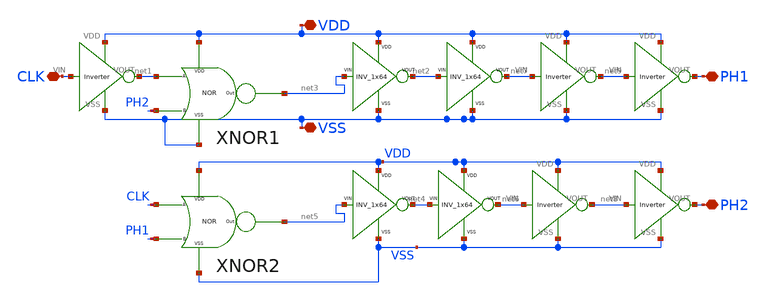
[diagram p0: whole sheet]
** sch_path: xschem/xschem_BGR_Top/Sigma_Delta/Non_over_clk/Non_over_clk.sch
**.subckt Non_over_clk VDD VSS CLK PH1 PH2
*.iopin VDD
*.iopin VSS
*.iopin CLK
*.iopin PH1
*.iopin PH2
X1 VSS VDD CLK net1 Inverter
X2 VSS VDD net9 PH1 Inverter
X3 VSS VDD net8 PH2 Inverter
X4 VSS VDD net3 net2 INV_1x64
X5 VSS VDD net5 net4 INV_1x64
XNOR1 VDD VSS net1 PH2 net3 NOR
XNOR2 VDD VSS CLK PH1 net5 NOR
X8 VSS VDD net6 net8 Inverter
X9 VSS VDD net7 net9 Inverter
X6 VSS VDD net2 net7 INV_1x64
X7 VSS VDD net4 net6 INV_1x64
**.ends

* expanding   symbol:  Sigma_Delta/Inverter/Inverter.sym # of pins=4
** sym_path: xschem/xschem_BGR_Top/Sigma_Delta/Inverter/Inverter.sym
** sch_path: xschem/xschem_BGR_Top/Sigma_Delta/Inverter/Inverter.sch
.subckt Inverter VSS VDD VIN VOUT
*.ipin VIN
*.iopin VDD
*.iopin VSS
*.opin VOUT
XM1 VOUT VIN VSS VSS sky130_fd_pr__nfet_01v8 L=0.15 W=0.9 nf=1 ad='int((nf+1)/2) * W/nf * 0.29' as='int((nf+2)/2) * W/nf * 0.29'
+ pd='2*int((nf+1)/2) * (W/nf + 0.29)' ps='2*int((nf+2)/2) * (W/nf + 0.29)' nrd='0.29 / W' nrs='0.29 / W'
+ sa=0 sb=0 sd=0 mult=1 m=1
XM2 VOUT VIN VDD VDD sky130_fd_pr__pfet_01v8 L=0.15 W=0.9 nf=2 ad='int((nf+1)/2) * W/nf * 0.29' as='int((nf+2)/2) * W/nf * 0.29'
+ pd='2*int((nf+1)/2) * (W/nf + 0.29)' ps='2*int((nf+2)/2) * (W/nf + 0.29)' nrd='0.29 / W' nrs='0.29 / W'
+ sa=0 sb=0 sd=0 mult=1 m=1
.ends


* expanding   symbol:  Sigma_Delta/INV_1x64/INV_1x64.sym # of pins=4
** sym_path: xschem/xschem_BGR_Top/Sigma_Delta/INV_1x64/INV_1x64.sym
** sch_path: xschem/xschem_BGR_Top/Sigma_Delta/INV_1x64/INV_1x64.sch
.subckt INV_1x64 VSS VDD VIN VOUT
*.ipin VIN
*.iopin VDD
*.iopin VSS
*.opin VOUT
XM1 VOUT VIN net1 VSS sky130_fd_pr__nfet_01v8 L=0.15 W=0.425 nf=1 ad='int((nf+1)/2) * W/nf * 0.29' as='int((nf+2)/2) * W/nf * 0.29'
+ pd='2*int((nf+1)/2) * (W/nf + 0.29)' ps='2*int((nf+2)/2) * (W/nf + 0.29)' nrd='0.29 / W' nrs='0.29 / W'
+ sa=0 sb=0 sd=0 mult=1 m=1
XM2 VOUT VIN net2 VDD sky130_fd_pr__pfet_01v8 L=0.15 W=0.425 nf=1 ad='int((nf+1)/2) * W/nf * 0.29' as='int((nf+2)/2) * W/nf * 0.29'
+ pd='2*int((nf+1)/2) * (W/nf + 0.29)' ps='2*int((nf+2)/2) * (W/nf + 0.29)' nrd='0.29 / W' nrs='0.29 / W'
+ sa=0 sb=0 sd=0 mult=1 m=1
XM3 net2 VIN net3 VDD sky130_fd_pr__pfet_01v8 L=0.15 W=0.425 nf=1 ad='int((nf+1)/2) * W/nf * 0.29' as='int((nf+2)/2) * W/nf * 0.29'
+ pd='2*int((nf+1)/2) * (W/nf + 0.29)' ps='2*int((nf+2)/2) * (W/nf + 0.29)' nrd='0.29 / W' nrs='0.29 / W'
+ sa=0 sb=0 sd=0 mult=1 m=1
XM4 net3 VIN net4 VDD sky130_fd_pr__pfet_01v8 L=0.15 W=0.425 nf=1 ad='int((nf+1)/2) * W/nf * 0.29' as='int((nf+2)/2) * W/nf * 0.29'
+ pd='2*int((nf+1)/2) * (W/nf + 0.29)' ps='2*int((nf+2)/2) * (W/nf + 0.29)' nrd='0.29 / W' nrs='0.29 / W'
+ sa=0 sb=0 sd=0 mult=1 m=1
XM5 net4 VIN net8 VDD sky130_fd_pr__pfet_01v8 L=0.15 W=0.425 nf=1 ad='int((nf+1)/2) * W/nf * 0.29' as='int((nf+2)/2) * W/nf * 0.29'
+ pd='2*int((nf+1)/2) * (W/nf + 0.29)' ps='2*int((nf+2)/2) * (W/nf + 0.29)' nrd='0.29 / W' nrs='0.29 / W'
+ sa=0 sb=0 sd=0 mult=1 m=1
XM6 net1 VIN net5 VSS sky130_fd_pr__nfet_01v8 L=0.15 W=0.425 nf=1 ad='int((nf+1)/2) * W/nf * 0.29' as='int((nf+2)/2) * W/nf * 0.29'
+ pd='2*int((nf+1)/2) * (W/nf + 0.29)' ps='2*int((nf+2)/2) * (W/nf + 0.29)' nrd='0.29 / W' nrs='0.29 / W'
+ sa=0 sb=0 sd=0 mult=1 m=1
XM7 net5 VIN net6 VSS sky130_fd_pr__nfet_01v8 L=0.15 W=0.425 nf=1 ad='int((nf+1)/2) * W/nf * 0.29' as='int((nf+2)/2) * W/nf * 0.29'
+ pd='2*int((nf+1)/2) * (W/nf + 0.29)' ps='2*int((nf+2)/2) * (W/nf + 0.29)' nrd='0.29 / W' nrs='0.29 / W'
+ sa=0 sb=0 sd=0 mult=1 m=1
XM8 net6 VIN net7 VSS sky130_fd_pr__nfet_01v8 L=0.15 W=0.425 nf=1 ad='int((nf+1)/2) * W/nf * 0.29' as='int((nf+2)/2) * W/nf * 0.29'
+ pd='2*int((nf+1)/2) * (W/nf + 0.29)' ps='2*int((nf+2)/2) * (W/nf + 0.29)' nrd='0.29 / W' nrs='0.29 / W'
+ sa=0 sb=0 sd=0 mult=1 m=1
XM9 net7 VIN VSS VSS sky130_fd_pr__nfet_01v8 L=0.15 W=0.425 nf=1 ad='int((nf+1)/2) * W/nf * 0.29' as='int((nf+2)/2) * W/nf * 0.29'
+ pd='2*int((nf+1)/2) * (W/nf + 0.29)' ps='2*int((nf+2)/2) * (W/nf + 0.29)' nrd='0.29 / W' nrs='0.29 / W'
+ sa=0 sb=0 sd=0 mult=1 m=1
XM10 net8 VIN VDD VDD sky130_fd_pr__pfet_01v8 L=0.15 W=0.425 nf=1 ad='int((nf+1)/2) * W/nf * 0.29' as='int((nf+2)/2) * W/nf * 0.29'
+ pd='2*int((nf+1)/2) * (W/nf + 0.29)' ps='2*int((nf+2)/2) * (W/nf + 0.29)' nrd='0.29 / W' nrs='0.29 / W'
+ sa=0 sb=0 sd=0 mult=1 m=1
.ends


* expanding   symbol:  Sigma_Delta/Nor/NOR.sym # of pins=5
** sym_path: xschem/xschem_BGR_Top/Sigma_Delta/Nor/NOR.sym
** sch_path: xschem/xschem_BGR_Top/Sigma_Delta/Nor/NOR.sch
.subckt NOR VDD VSS A B OUT
*.iopin VDD
*.iopin VSS
*.iopin A
*.iopin B
*.iopin OUT
XM2 OUT A VSS VSS sky130_fd_pr__nfet_01v8 L=0.15 W=0.5 nf=1 ad='int((nf+1)/2) * W/nf * 0.29' as='int((nf+2)/2) * W/nf * 0.29'
+ pd='2*int((nf+1)/2) * (W/nf + 0.29)' ps='2*int((nf+2)/2) * (W/nf + 0.29)' nrd='0.29 / W' nrs='0.29 / W'
+ sa=0 sb=0 sd=0 mult=1 m=1
XM3 net1 A VDD VDD sky130_fd_pr__pfet_01v8 L=0.15 W=0.5 nf=1 ad='int((nf+1)/2) * W/nf * 0.29' as='int((nf+2)/2) * W/nf * 0.29'
+ pd='2*int((nf+1)/2) * (W/nf + 0.29)' ps='2*int((nf+2)/2) * (W/nf + 0.29)' nrd='0.29 / W' nrs='0.29 / W'
+ sa=0 sb=0 sd=0 mult=1 m=1
XM1 OUT B net1 VDD sky130_fd_pr__pfet_01v8 L=0.15 W=0.5 nf=1 ad='int((nf+1)/2) * W/nf * 0.29' as='int((nf+2)/2) * W/nf * 0.29'
+ pd='2*int((nf+1)/2) * (W/nf + 0.29)' ps='2*int((nf+2)/2) * (W/nf + 0.29)' nrd='0.29 / W' nrs='0.29 / W'
+ sa=0 sb=0 sd=0 mult=1 m=1
XM4 OUT B VSS VSS sky130_fd_pr__nfet_01v8 L=0.15 W=0.5 nf=1 ad='int((nf+1)/2) * W/nf * 0.29' as='int((nf+2)/2) * W/nf * 0.29'
+ pd='2*int((nf+1)/2) * (W/nf + 0.29)' ps='2*int((nf+2)/2) * (W/nf + 0.29)' nrd='0.29 / W' nrs='0.29 / W'
+ sa=0 sb=0 sd=0 mult=1 m=1
.ends

.end
